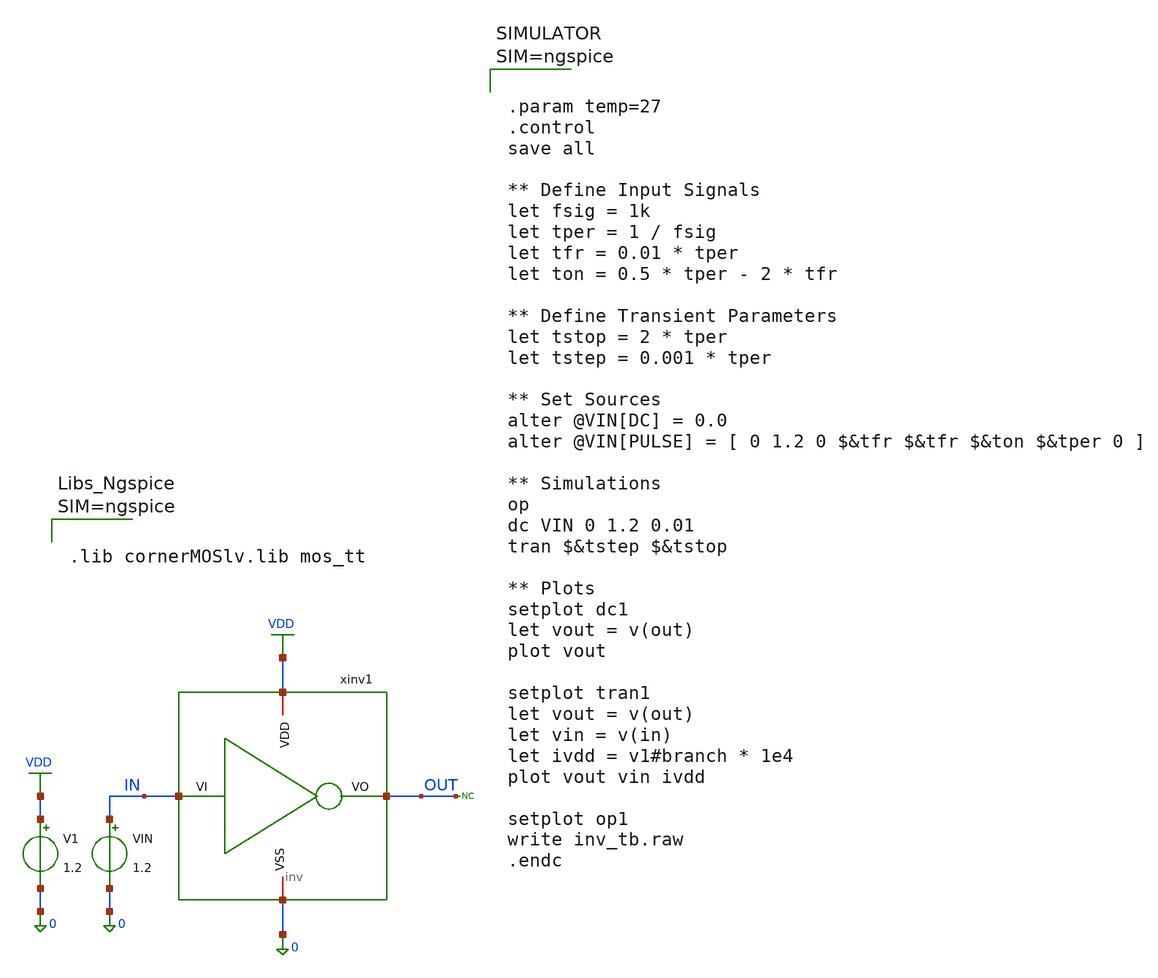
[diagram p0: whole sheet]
** sch_path: designs/archives/inv/inv_tb.sch
**.subckt inv_tb
V1 VDD 0 1.2
VIN IN 0 1.2
xinv1 VDD IN OUT 0 inv
* noconn OUT
**** begin user architecture code



.lib cornerMOSlv.lib mos_tt






.param temp=27
.control
save all

** Define Input Signals
let fsig = 1k
let tper = 1 / fsig
let tfr = 0.01 * tper
let ton = 0.5 * tper - 2 * tfr

** Define Transient Parameters
let tstop = 2 * tper
let tstep = 0.001 * tper

** Set Sources
alter @VIN[DC] = 0.0
alter @VIN[PULSE] = [ 0 1.2 0 $&tfr $&tfr $&ton $&tper 0 ]

** Simulations
op
dc VIN 0 1.2 0.01
tran $&tstep $&tstop

** Plots
setplot dc1
let vout = v(out)
plot vout

setplot tran1
let vout = v(out)
let vin = v(in)
let ivdd = v1#branch * 1e4
plot vout vin ivdd

setplot op1
write inv_tb.raw
.endc



**** end user architecture code
**.ends

* expanding   symbol:  inv.sym # of pins=4
** sym_path: designs/archives/inv/inv.sym
** sch_path: designs/archives/inv/inv.sch
.subckt inv VDD VI VO VSS
*.iopin VDD
*.iopin VSS
*.ipin VI
*.opin VO
XM1 VO VI VSS VSS sg13_lv_nmos w=0.15u l=0.13u ng=1 m=1 mm_ok=1
XM2 VO VI VDD VDD sg13_lv_pmos w=0.15u l=0.13u ng=1 m=1 mm_ok=1
.ends

.GLOBAL VDD
.end
